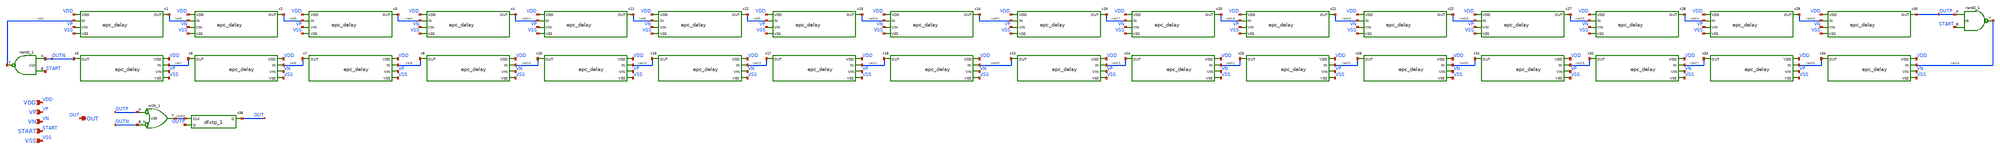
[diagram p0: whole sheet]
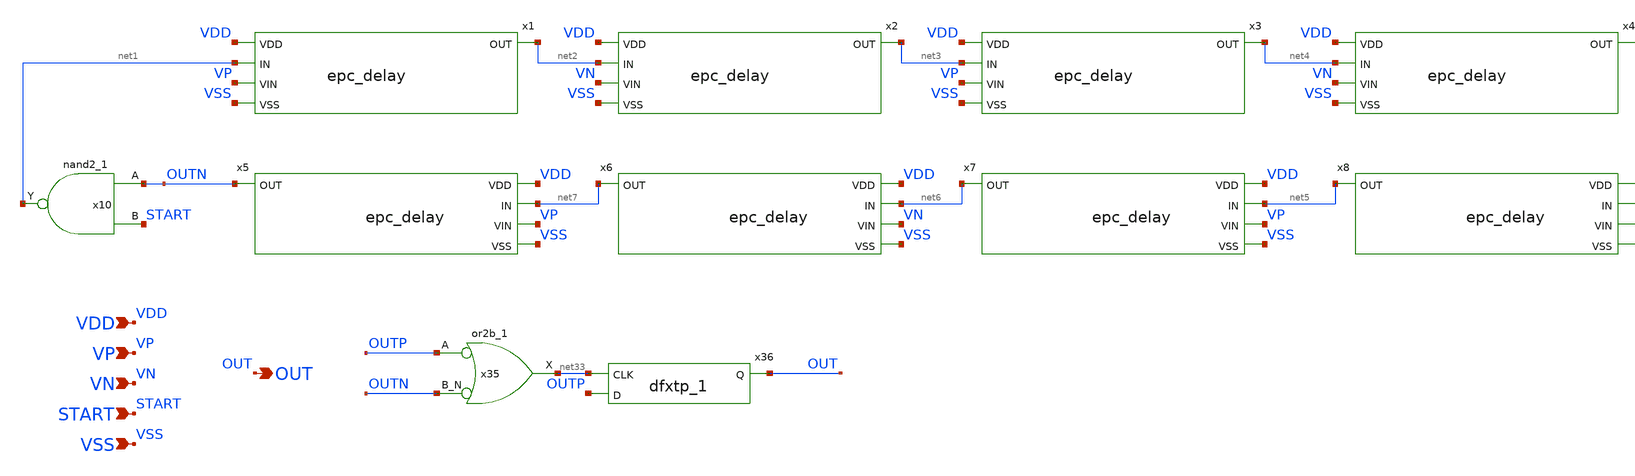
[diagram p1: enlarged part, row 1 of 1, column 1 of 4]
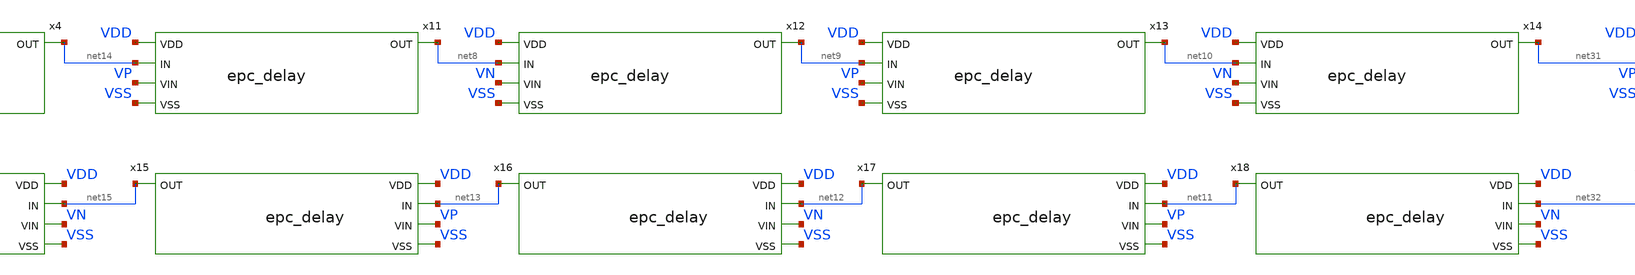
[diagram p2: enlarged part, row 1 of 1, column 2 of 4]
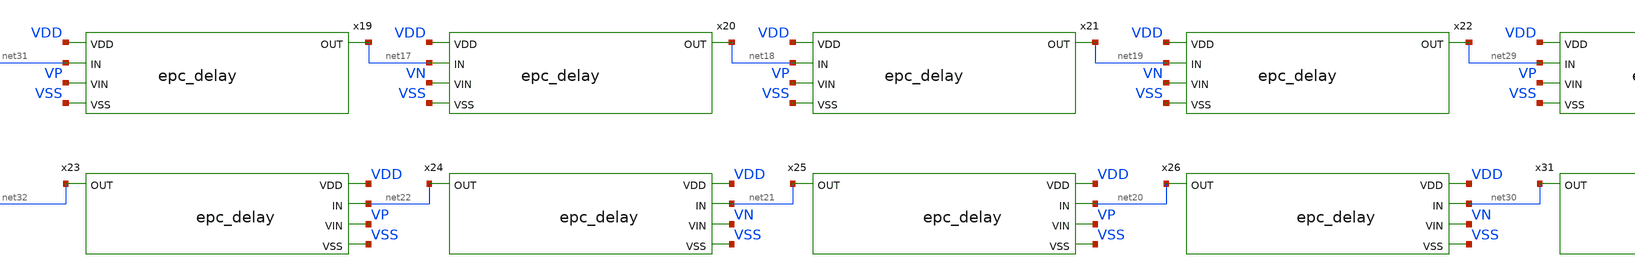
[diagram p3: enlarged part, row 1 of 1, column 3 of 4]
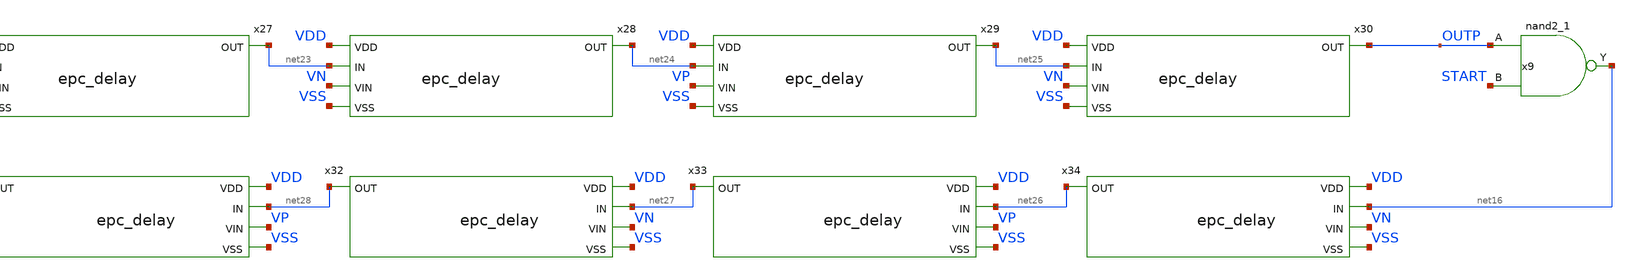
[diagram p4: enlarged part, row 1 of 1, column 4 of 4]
** sch_path: xschem/epc.sch
**.subckt epc VDD VP VN VSS OUT START
*.ipin VDD
*.ipin VP
*.ipin VN
*.ipin VSS
*.opin OUT
*.ipin START
x1 VDD net1 net2 VP VSS epc_delay
x2 VDD net2 net3 VN VSS epc_delay
x3 VDD net3 net4 VP VSS epc_delay
x4 VDD net4 net14 VN VSS epc_delay
x5 VDD net7 OUTN VP VSS epc_delay
x6 VDD net6 net7 VN VSS epc_delay
x7 VDD net5 net6 VP VSS epc_delay
x8 VDD net15 net5 VN VSS epc_delay
x9 OUTP START VSS VSS VDD VDD net16 sky130_fd_sc_hd__nand2_1
x10 OUTN START VSS VSS VDD VDD net1 sky130_fd_sc_hd__nand2_1
x11 VDD net14 net8 VP VSS epc_delay
x12 VDD net8 net9 VN VSS epc_delay
x13 VDD net9 net10 VP VSS epc_delay
x14 VDD net10 net31 VN VSS epc_delay
x15 VDD net13 net15 VP VSS epc_delay
x16 VDD net12 net13 VN VSS epc_delay
x17 VDD net11 net12 VP VSS epc_delay
x18 VDD net32 net11 VN VSS epc_delay
x19 VDD net31 net17 VP VSS epc_delay
x20 VDD net17 net18 VN VSS epc_delay
x21 VDD net18 net19 VP VSS epc_delay
x22 VDD net19 net29 VN VSS epc_delay
x23 VDD net22 net32 VP VSS epc_delay
x24 VDD net21 net22 VN VSS epc_delay
x25 VDD net20 net21 VP VSS epc_delay
x26 VDD net30 net20 VN VSS epc_delay
x27 VDD net29 net23 VP VSS epc_delay
x28 VDD net23 net24 VN VSS epc_delay
x29 VDD net24 net25 VP VSS epc_delay
x30 VDD net25 OUTP VN VSS epc_delay
x31 VDD net28 net30 VP VSS epc_delay
x32 VDD net27 net28 VN VSS epc_delay
x33 VDD net26 net27 VP VSS epc_delay
x34 VDD net16 net26 VN VSS epc_delay
x35 OUTP OUTN VSS VSS VDD VDD net33 sky130_fd_sc_hd__or2b_1
x36 net33 OUTP VSS VSS VDD VDD OUT sky130_fd_sc_hd__dfxtp_1
**.ends
.end
